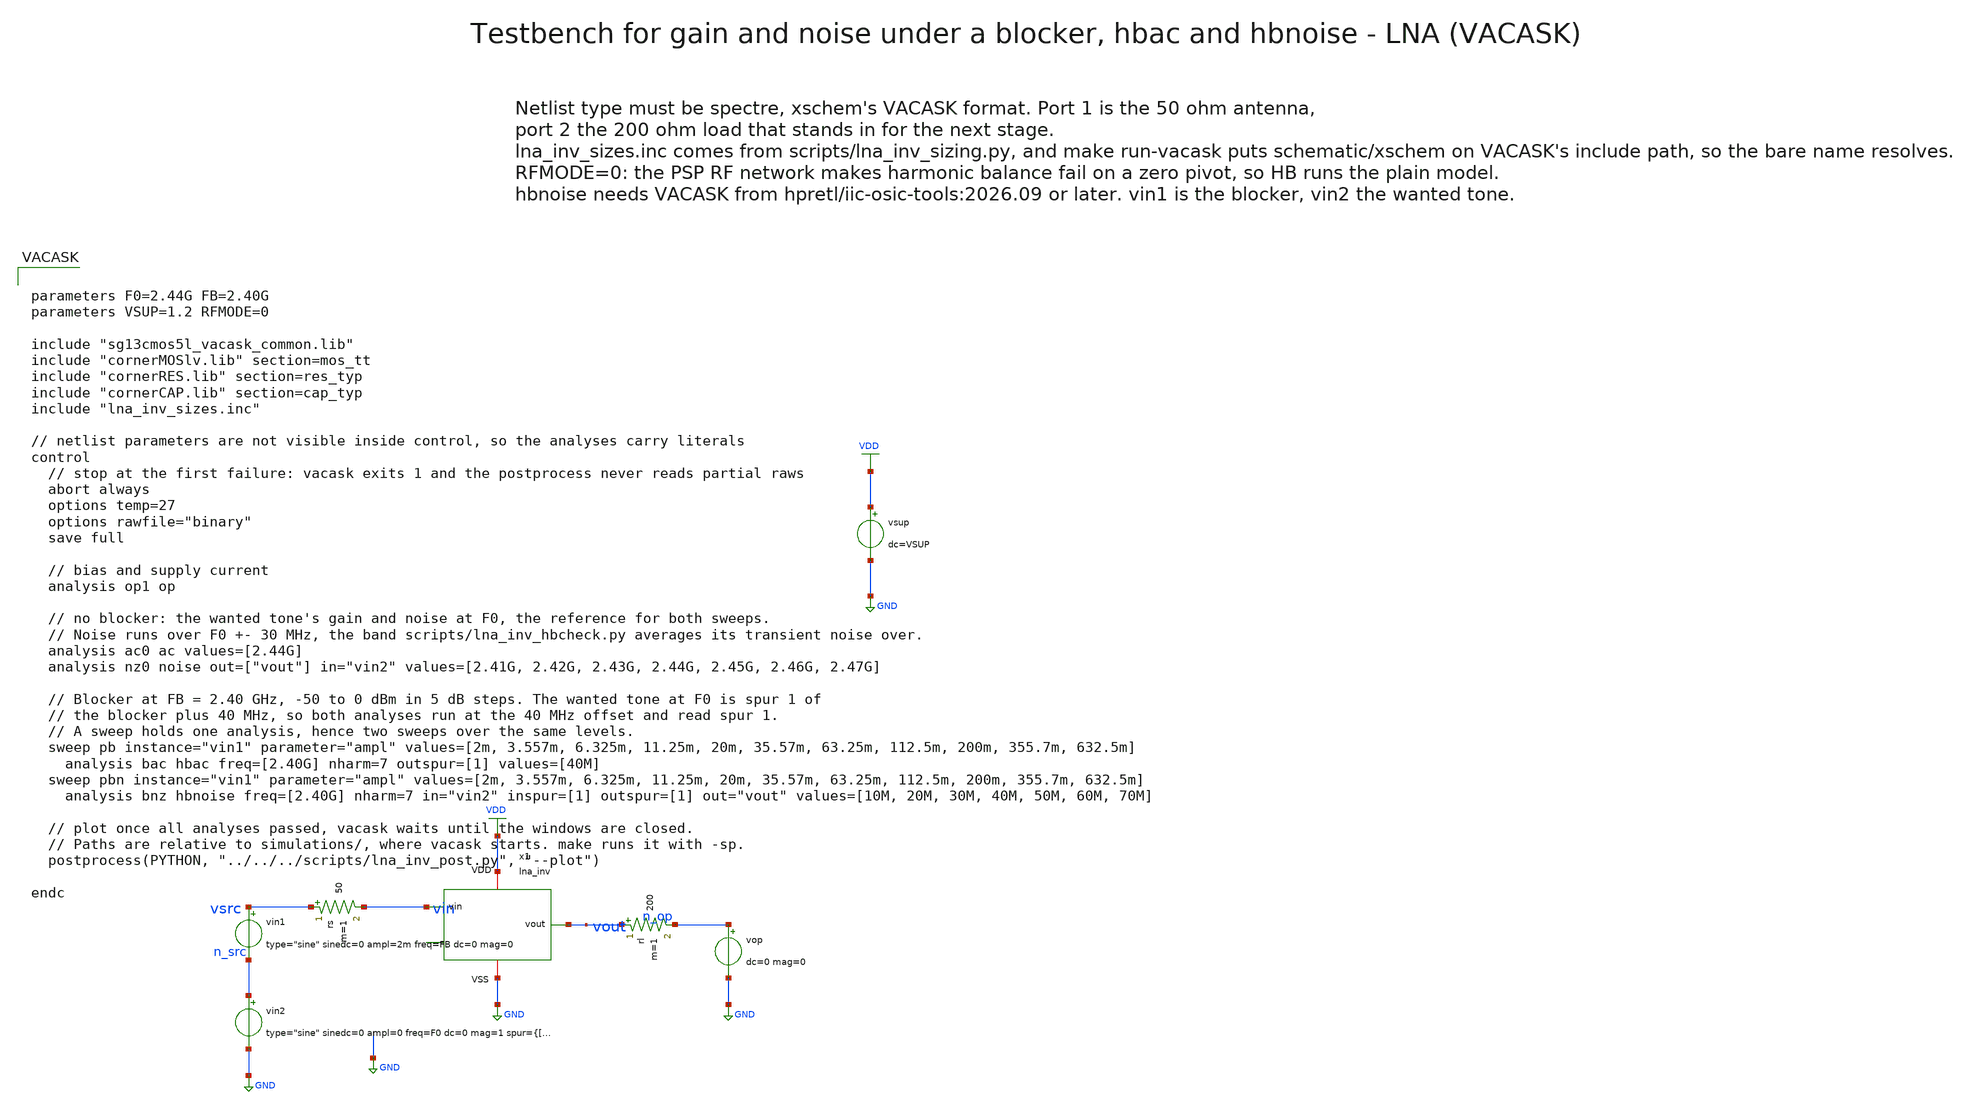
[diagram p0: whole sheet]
** sch_path: macros/lna_inv/testbenches/xschem/lna_inv_tb_blocker.sch
**.subckt lna_inv_tb_blocker
vin1 vsrc n_src type="sine" sinedc=0 ampl=2m freq=FB dc=0 mag=0
vin2 n_src GND type="sine" sinedc=0 ampl=0 freq=F0 dc=0 mag=1 spur={[1]} smag=[1]
rs vsrc vin 50 m=1
x1 vin vout VDD GND lna_inv
rl vout n_op 200 m=1
vop n_op GND dc=0 mag=0
vsup VDD GND dc=VSUP
**** begin user architecture code


parameters F0=2.44G FB=2.40G
parameters VSUP=1.2 RFMODE=0

include "sg13cmos5l_vacask_common.lib"
include "cornerMOSlv.lib" section=mos_tt
include "cornerRES.lib" section=res_typ
include "cornerCAP.lib" section=cap_typ
include "lna_inv_sizes.inc"

// netlist parameters are not visible inside control, so the analyses carry literals
control
  // stop at the first failure: vacask exits 1 and the postprocess never reads partial raws
  abort always
  options temp=27
  options rawfile="binary"
  save full

  // bias and supply current
  analysis op1 op

  // no blocker: the wanted tone's gain and noise at F0, the reference for both sweeps.
  // Noise runs over F0 +- 30 MHz, the band scripts/lna_inv_hbcheck.py averages its transient noise over.
  analysis ac0 ac values=[2.44G]
  analysis nz0 noise out=["vout"] in="vin2" values=[2.41G, 2.42G, 2.43G, 2.44G, 2.45G, 2.46G, 2.47G]

  // Blocker at FB = 2.40 GHz, -50 to 0 dBm in 5 dB steps. The wanted tone at F0 is spur 1 of
  // the blocker plus 40 MHz, so both analyses run at the 40 MHz offset and read spur 1.
  // A sweep holds one analysis, hence two sweeps over the same levels.
  sweep pb instance="vin1" parameter="ampl" values=[2m, 3.557m, 6.325m, 11.25m, 20m, 35.57m, 63.25m, 112.5m, 200m, 355.7m, 632.5m]
    analysis bac hbac freq=[2.40G] nharm=7 outspur=[1] values=[40M]
  sweep pbn instance="vin1" parameter="ampl" values=[2m, 3.557m, 6.325m, 11.25m, 20m, 35.57m, 63.25m, 112.5m, 200m, 355.7m, 632.5m]
    analysis bnz hbnoise freq=[2.40G] nharm=7 in="vin2" inspur=[1] outspur=[1] out="vout" values=[10M, 20M, 30M, 40M, 50M, 60M, 70M]

  // plot once all analyses passed, vacask waits until the windows are closed.
  // Paths are relative to simulations/, where vacask starts. make runs it with -sp.
  postprocess(PYTHON, "../../../scripts/lna_inv_post.py", "--plot")

endc


**** end user architecture code
**.ends
.GLOBAL GND
.GLOBAL VDD
.end
